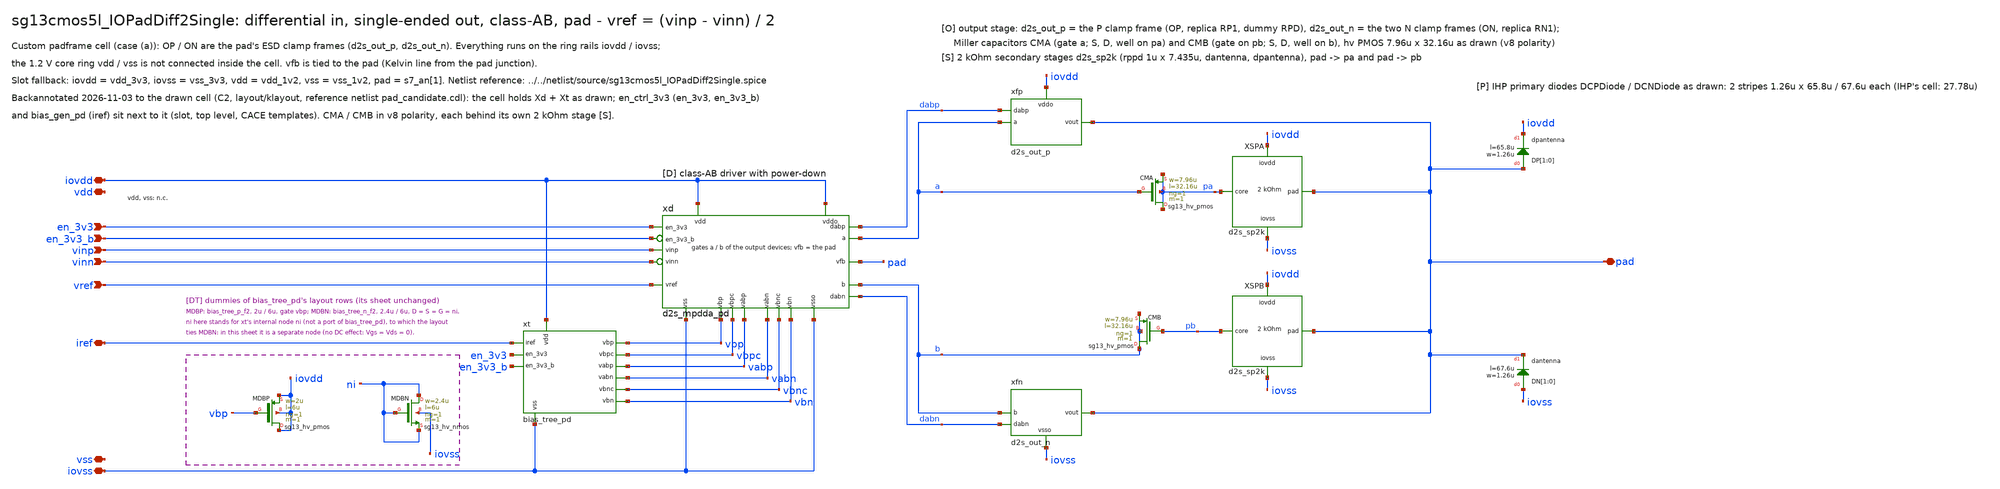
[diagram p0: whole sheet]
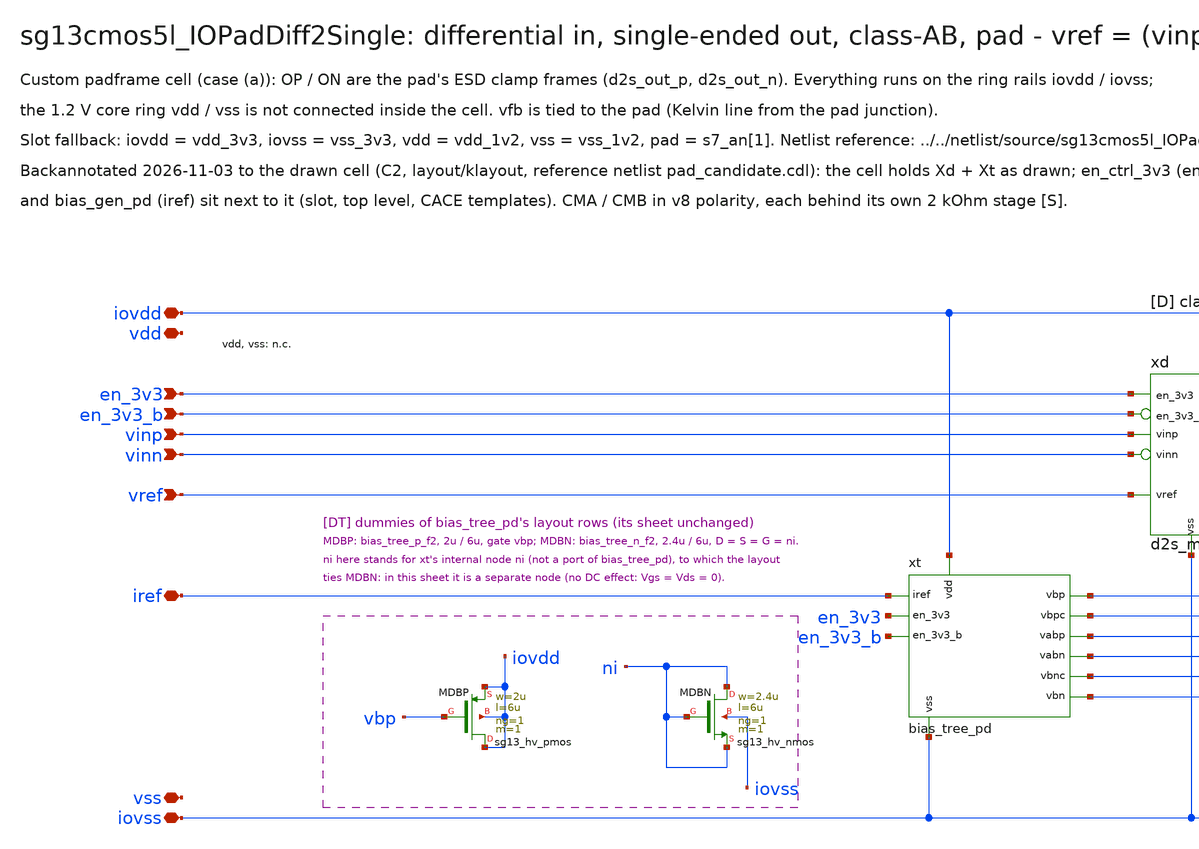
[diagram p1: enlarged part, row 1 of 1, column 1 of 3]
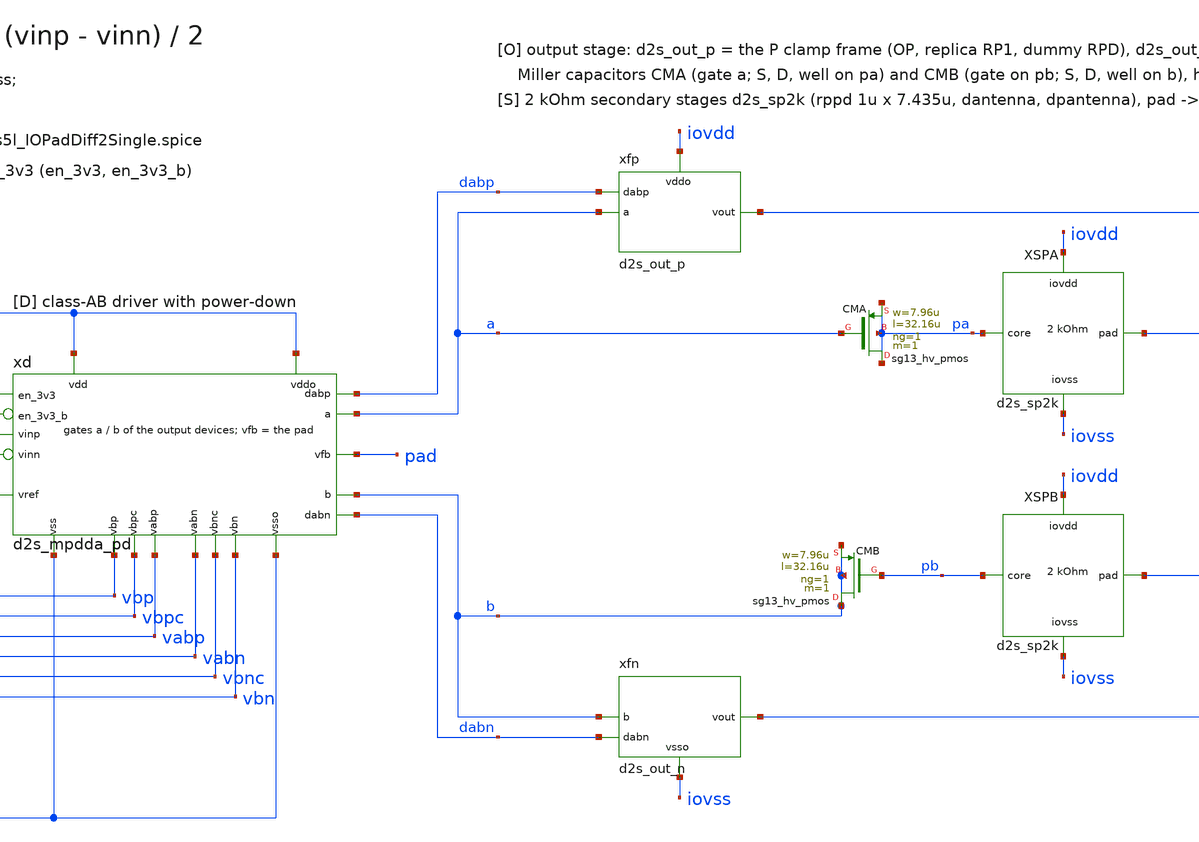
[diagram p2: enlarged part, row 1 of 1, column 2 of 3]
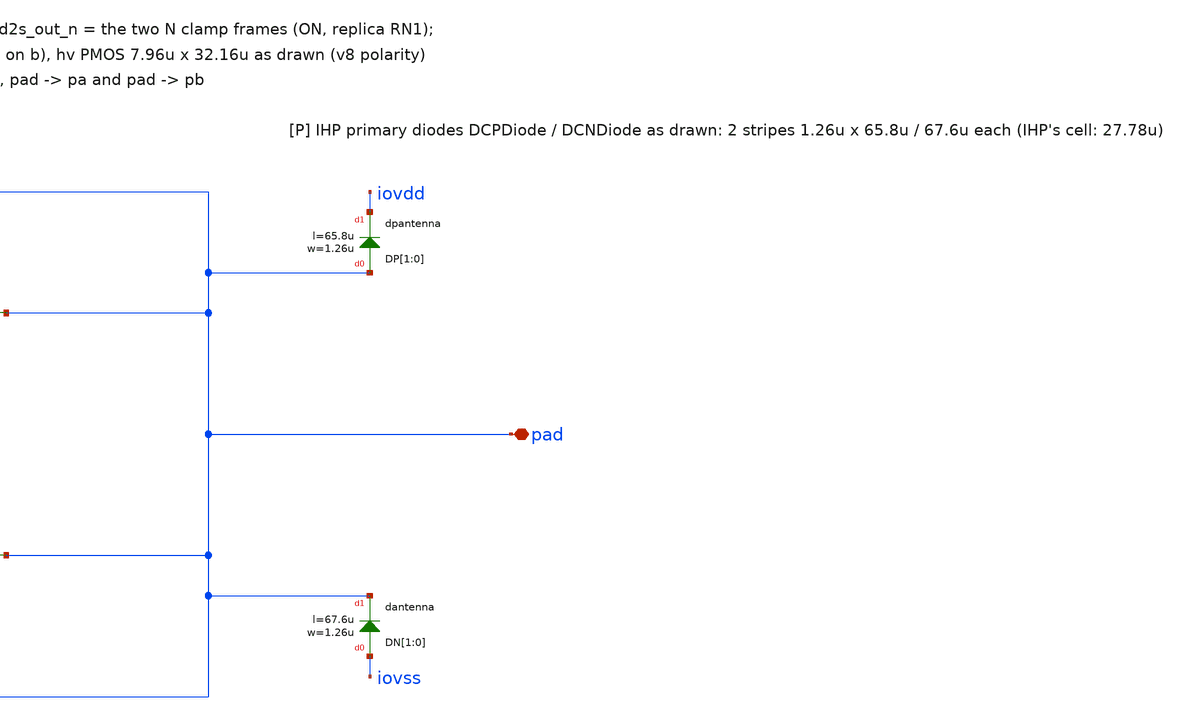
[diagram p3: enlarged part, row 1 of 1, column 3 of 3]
** sch_path: macros/sg13cmos5l_IOPadDiff2Single/schematic/xschem/sg13cmos5l_IOPadDiff2Single.sch
**.subckt sg13cmos5l_IOPadDiff2Single iovdd iovss vdd vss pad vinp vinn vref iref en_3v3 en_3v3_b
*.iopin iovdd
*.iopin iovss
*.iopin vdd
*.iopin vss
*.iopin pad
*.ipin vinp
*.ipin vinn
*.ipin vref
*.iopin iref
*.ipin en_3v3
*.ipin en_3v3_b
xt iovdd iovss iref vbp vbn vbpc vbnc vabp vabn en_3v3 en_3v3_b bias_tree_pd
xd iovdd iovss iovdd iovss vinp vinn vref pad a b dabp dabn vbp vbn vbpc vbnc vabp vabn en_3v3
+ en_3v3_b d2s_mpdda_pd
xfp iovdd a pad dabp d2s_out_p
xfn iovss b pad dabn d2s_out_n
XCMA pa a pa pa sg13_hv_pmos w=7.96u l=32.16u ng=1 m=1 mm_ok=1
XSPA pa iovdd iovss pad d2s_sp2k
XCMB b pb b b sg13_hv_pmos w=7.96u l=32.16u ng=1 m=1 mm_ok=1
XSPB pb iovdd iovss pad d2s_sp2k
XDP[1] pad iovdd dpantenna l=65.8u w=1.26u
XDP[0] pad iovdd dpantenna l=65.8u w=1.26u
XDN[1] iovss pad dantenna l=67.6u w=1.26u
XDN[0] iovss pad dantenna l=67.6u w=1.26u
XMDBP iovdd vbp iovdd iovdd sg13_hv_pmos w=2u l=6u ng=1 m=1 mm_ok=1
XMDBN ni ni ni iovss sg13_hv_nmos w=2.4u l=6u ng=1 m=1 mm_ok=1
**.ends
.end
